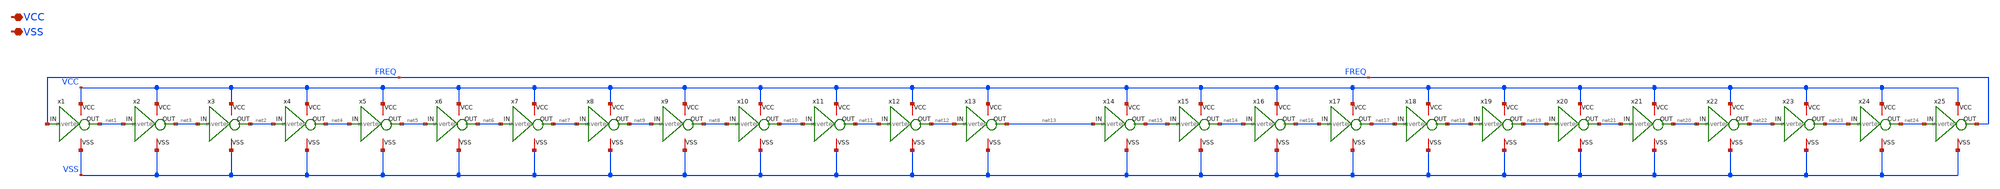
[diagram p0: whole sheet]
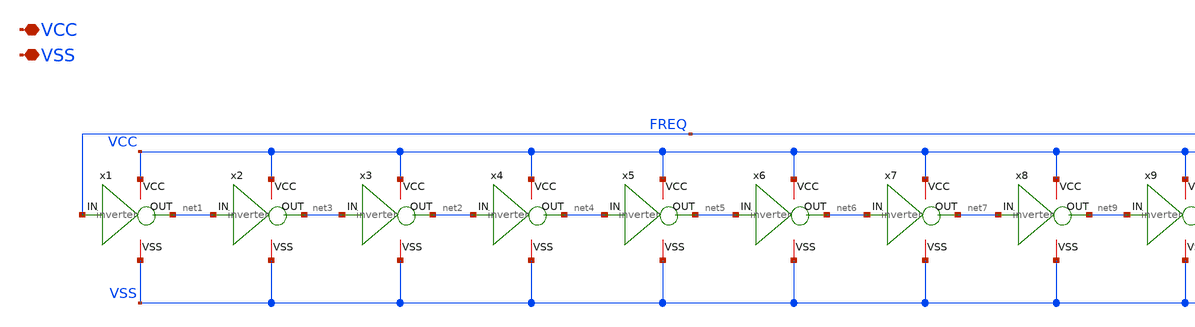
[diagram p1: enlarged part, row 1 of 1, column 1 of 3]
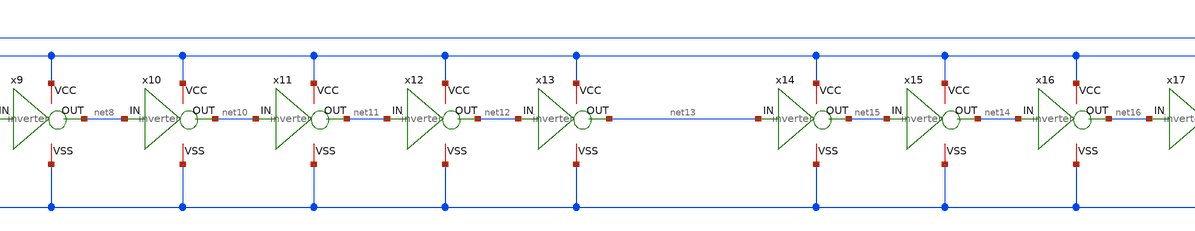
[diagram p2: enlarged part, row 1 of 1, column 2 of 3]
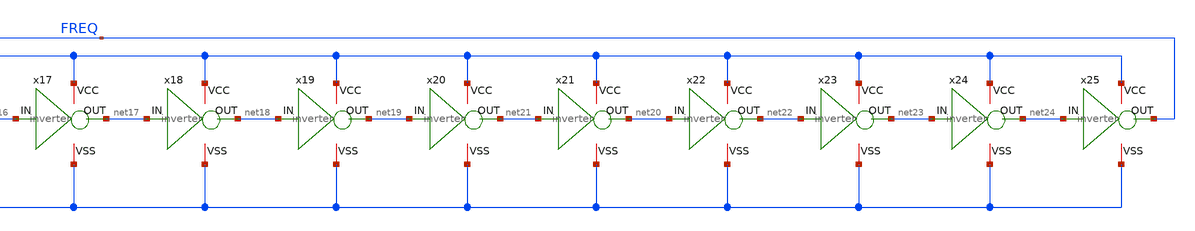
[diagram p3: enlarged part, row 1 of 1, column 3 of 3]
** sch_path: xschem/inverter_tb.sch
**.subckt inverter_tb VCC VSS
*.iopin VCC
*.iopin VSS
x1 net1 FREQ VCC VSS inverter
x2 net3 net1 VCC VSS inverter
x3 net2 net3 VCC VSS inverter
x4 net4 net2 VCC VSS inverter
x5 net5 net4 VCC VSS inverter
x6 net6 net5 VCC VSS inverter
x7 net7 net6 VCC VSS inverter
x8 net9 net7 VCC VSS inverter
x9 net8 net9 VCC VSS inverter
x10 net10 net8 VCC VSS inverter
x11 net11 net10 VCC VSS inverter
x12 net12 net11 VCC VSS inverter
x13 net13 net12 VCC VSS inverter
x14 net15 net13 VCC VSS inverter
x15 net14 net15 VCC VSS inverter
x16 net16 net14 VCC VSS inverter
x17 net17 net16 VCC VSS inverter
x18 net18 net17 VCC VSS inverter
x19 net19 net18 VCC VSS inverter
x20 net21 net19 VCC VSS inverter
x21 net20 net21 VCC VSS inverter
x22 net22 net20 VCC VSS inverter
x23 net23 net22 VCC VSS inverter
x24 net24 net23 VCC VSS inverter
x25 FREQ net24 VCC VSS inverter
**** begin user architecture code

** opencircuitdesign pdks install
.lib $::SKYWATER_MODELS/sky130.lib.spice tt





* ngspice commands
.param VCC=1.8
vvss vss 0 dc 0
vvcc vcc 0 pwl 0 0 10n 0 10.1n VCC 200n VCC

.control
tran 100p 200n
write inverter_tb.raw
.endc




**** end user architecture code
**.ends

* expanding   symbol:  inverter.sym # of pins=4
** sym_path: xschem/inverter.sym
** sch_path: xschem/inverter.sch
.subckt inverter OUT IN VCC VSS
*.iopin VCC
*.iopin VSS
*.ipin IN
*.opin OUT
XM1 OUT IN net1 VCC sky130_fd_pr__pfet_01v8 L=1 W=2 nf=1 ad='int((nf+1)/2) * W/nf * 0.29' as='int((nf+2)/2) * W/nf * 0.29'
+ pd='2*int((nf+1)/2) * (W/nf + 0.29)' ps='2*int((nf+2)/2) * (W/nf + 0.29)' nrd='0.29 / W' nrs='0.29 / W'
+ sa=0 sb=0 sd=0 mult=1 m=1
XM2 OUT IN net2 VSS sky130_fd_pr__nfet_01v8 L=1 W=1 nf=1 ad='int((nf+1)/2) * W/nf * 0.29' as='int((nf+2)/2) * W/nf * 0.29'
+ pd='2*int((nf+1)/2) * (W/nf + 0.29)' ps='2*int((nf+2)/2) * (W/nf + 0.29)' nrd='0.29 / W' nrs='0.29 / W'
+ sa=0 sb=0 sd=0 mult=1 m=1
XM3 net1 VSS VCC VCC sky130_fd_pr__pfet_01v8 L=1 W=2 nf=1 ad='int((nf+1)/2) * W/nf * 0.29' as='int((nf+2)/2) * W/nf * 0.29'
+ pd='2*int((nf+1)/2) * (W/nf + 0.29)' ps='2*int((nf+2)/2) * (W/nf + 0.29)' nrd='0.29 / W' nrs='0.29 / W'
+ sa=0 sb=0 sd=0 mult=1 m=1
XM4 net2 VCC VSS VSS sky130_fd_pr__nfet_01v8 L=1 W=1 nf=1 ad='int((nf+1)/2) * W/nf * 0.29' as='int((nf+2)/2) * W/nf * 0.29'
+ pd='2*int((nf+1)/2) * (W/nf + 0.29)' ps='2*int((nf+2)/2) * (W/nf + 0.29)' nrd='0.29 / W' nrs='0.29 / W'
+ sa=0 sb=0 sd=0 mult=1 m=1
.ends

.end
